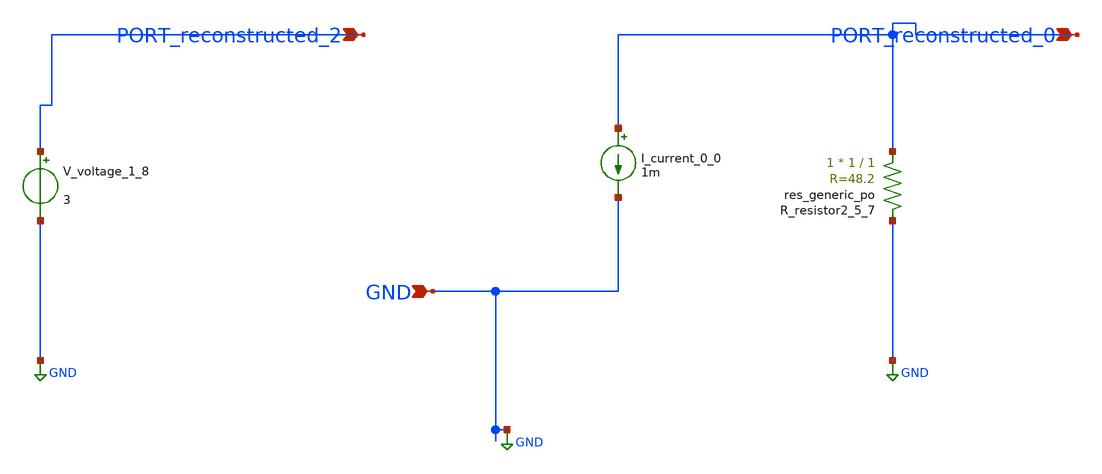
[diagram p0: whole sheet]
** sch_path: schematics/AMSNet/66.sch
**.subckt 66 PORT_reconstructed_0 GND PORT_reconstructed_2
*.ipin PORT_reconstructed_0
*.ipin GND
*.ipin PORT_reconstructed_2
I_current_0_0 PORT_reconstructed_0 GND 1m
XR_resistor2_5_7 PORT_reconstructed_0 GND sky130_fd_pr__res_generic_po W=1 L=1 m=1
V_voltage_1_8 PORT_reconstructed_2 GND 3
**.ends
.GLOBAL GND
.end
